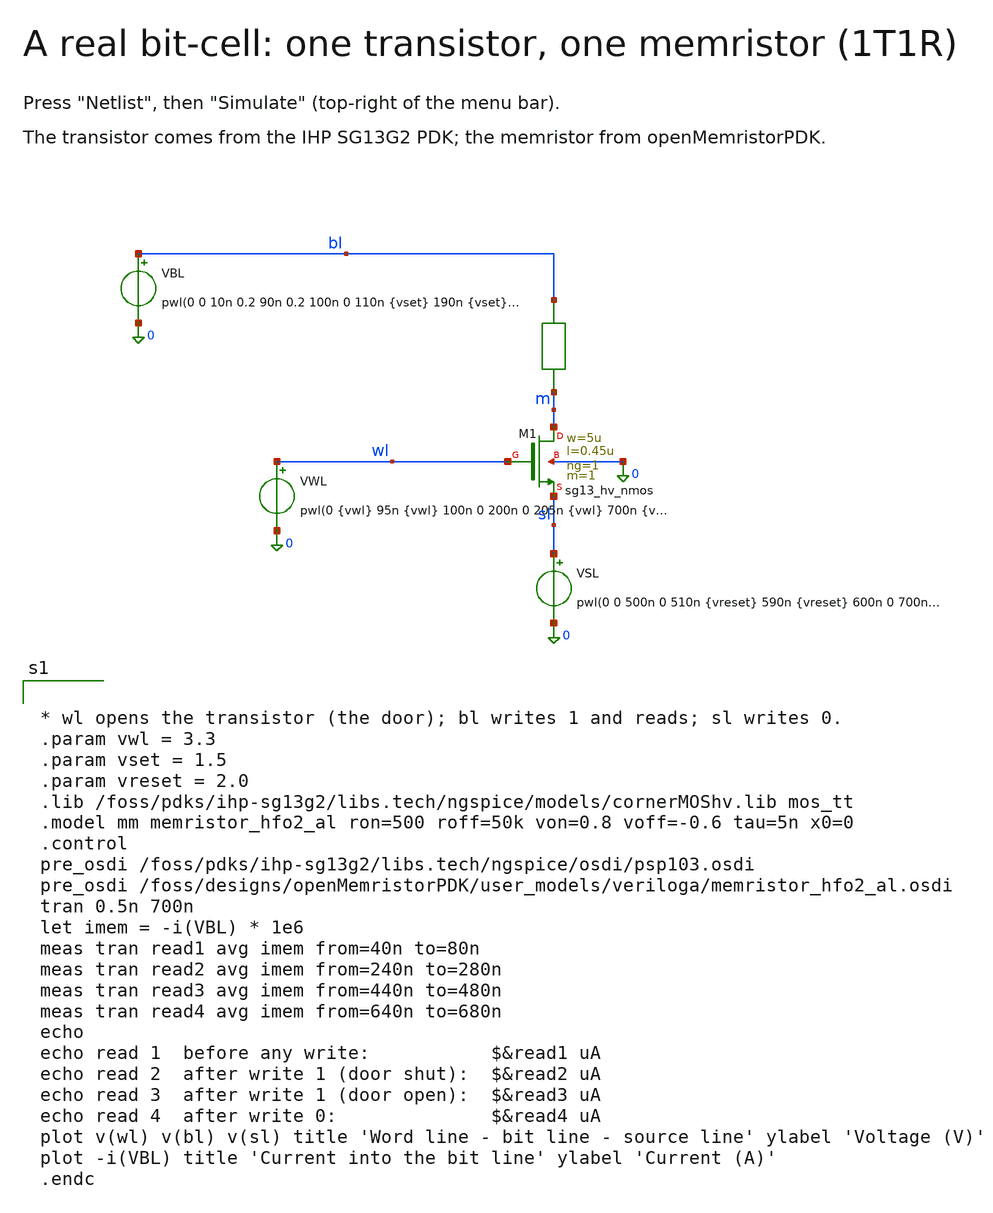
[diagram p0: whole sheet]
** sch_path: libraries/openmemristorpdk_pr/memristor_hfo2_al_1t1r_tb.sch
**.subckt memristor_hfo2_al_1t1r_tb
VBL bl 0 pwl(0 0 10n 0.2 90n 0.2 100n 0 110n {vset} 190n {vset} 200n 0 210n 0.2 290n 0.2 300n 0 310n
+ {vset} 390n {vset} 400n 0 410n 0.2 490n 0.2 500n 0 600n 0 610n 0.2 690n 0.2 700n 0)
n1 bl m mm
XM1 m wl sl 0 sg13_hv_nmos w=5u l=0.45u ng=1 m=1 mm_ok=1
VWL wl 0 pwl(0 {vwl} 95n {vwl} 100n 0 200n 0 205n {vwl} 700n {vwl})
VSL sl 0 pwl(0 0 500n 0 510n {vreset} 590n {vreset} 600n 0 700n 0)
**** begin user architecture code


* wl opens the transistor (the door); bl writes 1 and reads; sl writes 0.
.param vwl = 3.3
.param vset = 1.5
.param vreset = 2.0
.lib /foss/pdks/ihp-sg13g2/libs.tech/ngspice/models/cornerMOShv.lib mos_tt
.model mm memristor_hfo2_al ron=500 roff=50k von=0.8 voff=-0.6 tau=5n x0=0
.control
pre_osdi /foss/pdks/ihp-sg13g2/libs.tech/ngspice/osdi/psp103.osdi
pre_osdi /foss/designs/openMemristorPDK/user_models/veriloga/memristor_hfo2_al.osdi
tran 0.5n 700n
let imem = -i(VBL) * 1e6
meas tran read1 avg imem from=40n to=80n
meas tran read2 avg imem from=240n to=280n
meas tran read3 avg imem from=440n to=480n
meas tran read4 avg imem from=640n to=680n
echo
echo read 1  before any write:           $&read1 uA
echo read 2  after write 1 (door shut):  $&read2 uA
echo read 3  after write 1 (door open):  $&read3 uA
echo read 4  after write 0:              $&read4 uA
plot v(wl) v(bl) v(sl) title 'Word line - bit line - source line' ylabel 'Voltage (V)'
plot -i(VBL) title 'Current into the bit line' ylabel 'Current (A)'
.endc


**** end user architecture code
**.ends
.end
